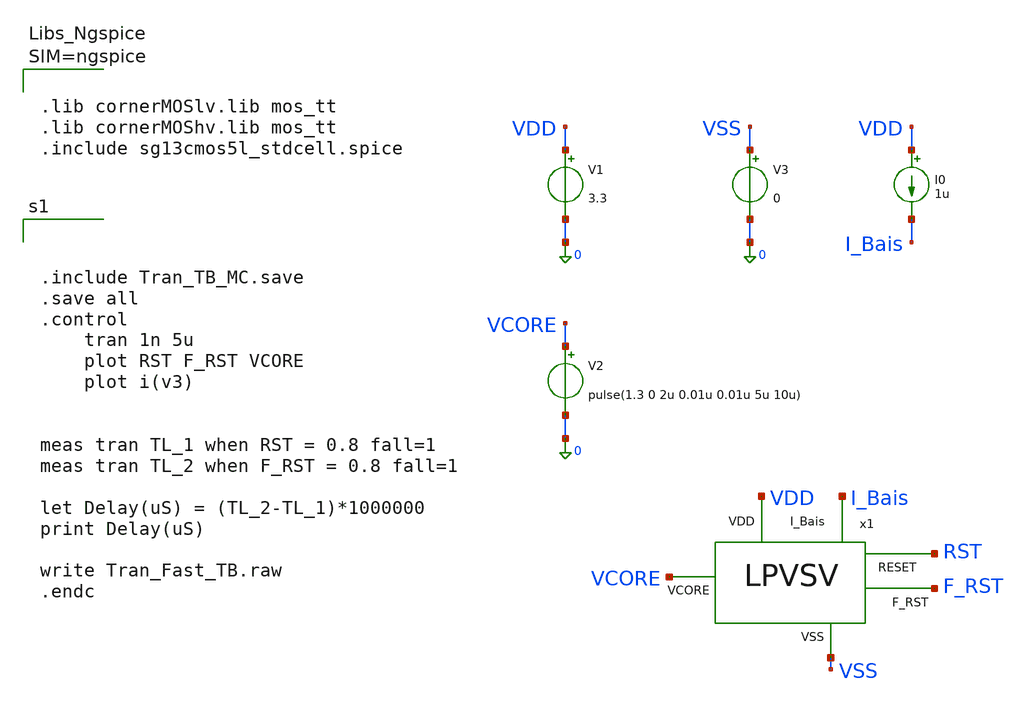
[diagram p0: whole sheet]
** sch_path: Simulation/Tran_Analysis/Tran_Fast_TB.sch
**.subckt Tran_Fast_TB
x1 VDD VCORE I_Bais RST F_RST VSS LPVSV
I0 VDD I_Bais 1u
V1 VDD 0 3.3
V2 VCORE 0 pulse(1.3 0 2u 0.01u 0.01u 5u 10u)
V3 VSS 0 0
**** begin user architecture code



.lib cornerMOSlv.lib mos_tt
.lib cornerMOShv.lib mos_tt
.include sg13cmos5l_stdcell.spice






.include Tran_TB_MC.save
.save all
.control
	tran 1n 5u
	plot RST F_RST VCORE
	plot i(v3)


meas tran TL_1 when RST = 0.8 fall=1
meas tran TL_2 when F_RST = 0.8 fall=1

let Delay(uS) = (TL_2-TL_1)*1000000
print Delay(uS)

write Tran_Fast_TB.raw
.endc


**** end user architecture code
**.ends
.end
